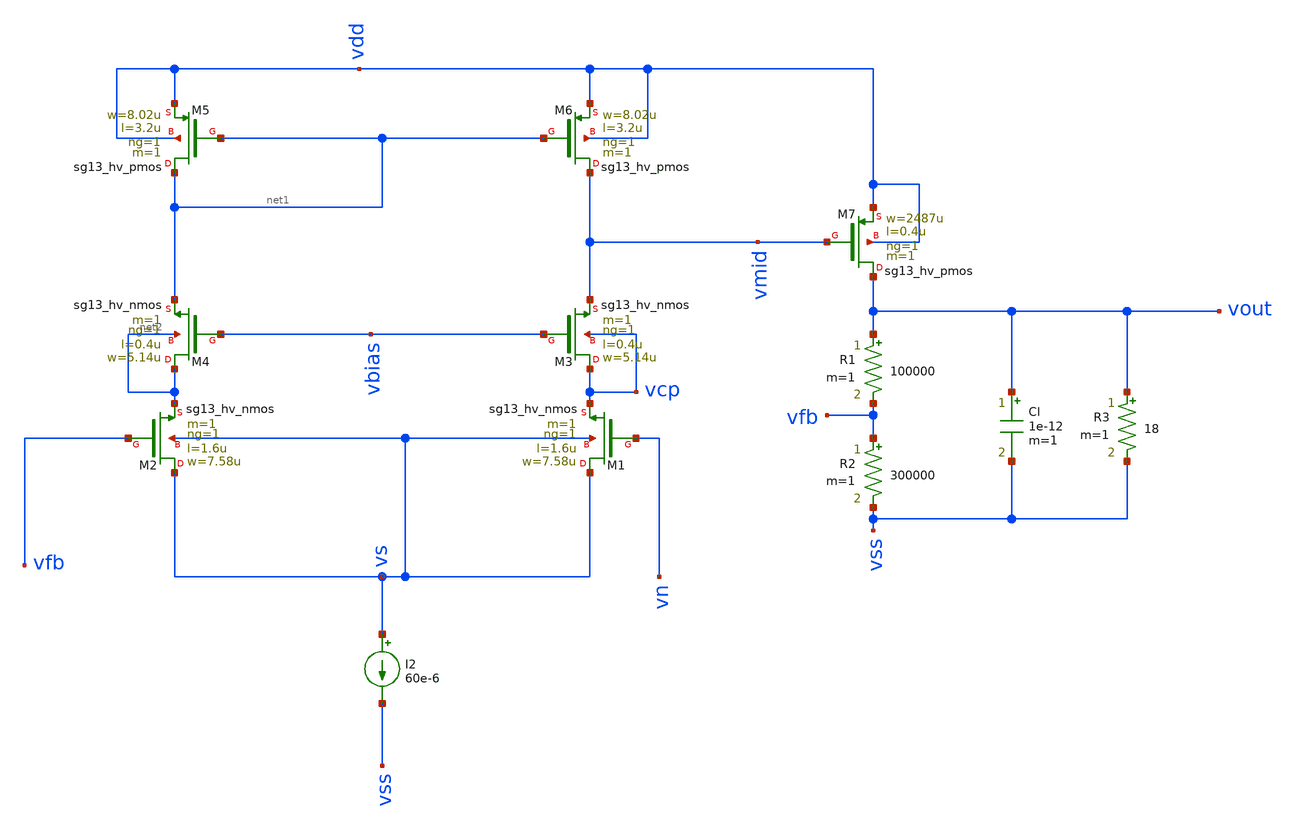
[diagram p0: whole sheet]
** sch_path: test-python/sstadex/xschem/ldo_sim_ihp_cc.sch
**.subckt ldo_sim_ihp_cc
R1 vout vfb 100000 m=1
R2 vfb vss 300000 m=1
Cl vout vss 1e-12 m=1
R3 vout vss 18 m=1
XM6 vmid net1 vdd vdd sg13_hv_pmos w=8.02u l=3.2u ng=1 m=1 mm_ok=1
I2 vs vss 60e-6
XM1 vs vn vcp vs sg13_hv_nmos w=7.58u l=1.6u ng=1 m=1 mm_ok=1
XM2 vs vfb net2 vs sg13_hv_nmos w=7.58u l=1.6u ng=1 m=1 mm_ok=1
XM3 vcp vbias vmid vcp sg13_hv_nmos w=5.14u l=0.4u ng=1 m=1 mm_ok=1
XM4 net2 vbias net1 net2 sg13_hv_nmos w=5.14u l=0.4u ng=1 m=1 mm_ok=1
XM5 net1 net1 vdd vdd sg13_hv_pmos w=8.02u l=3.2u ng=1 m=1 mm_ok=1
XM7 vout vmid vdd vdd sg13_hv_pmos w=2487u l=0.4u ng=1 m=1 mm_ok=1
**** begin user architecture code



.lib /opt/pdks/ihp-sg13g2/libs.tech/ngspice/models/cornerMOShv.lib mos_tt

Vref vn 0 1.35
Vdd vdd 0 3.3 ac 1
Vss vss 0 0
Vbias vbias 0 2.2

.control
ac dec 10 1 100G
plot vdb(vout)
plot phase(vout)
op
print vout vmid vcp vfb vs
.endc



**** end user architecture code
**.ends
.end
